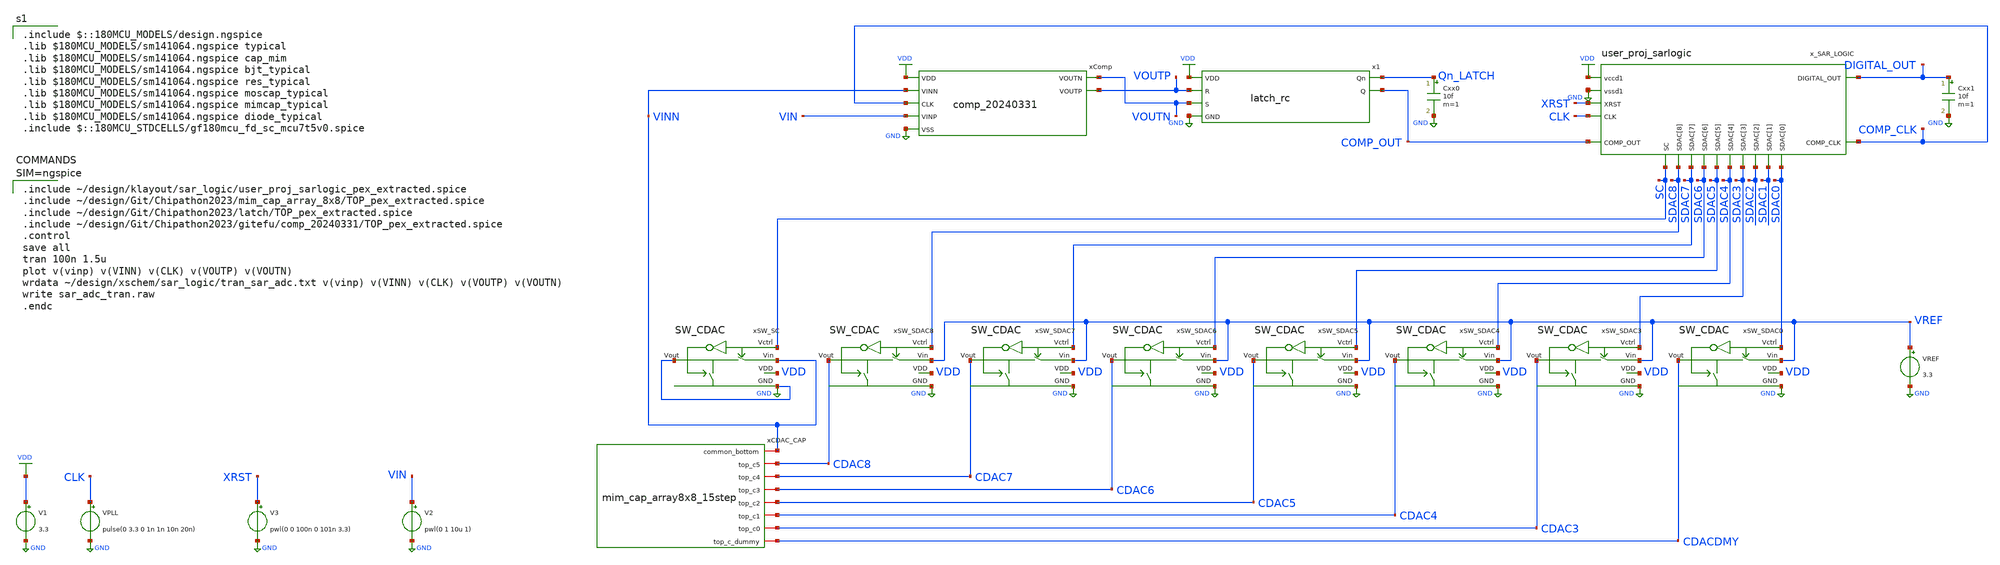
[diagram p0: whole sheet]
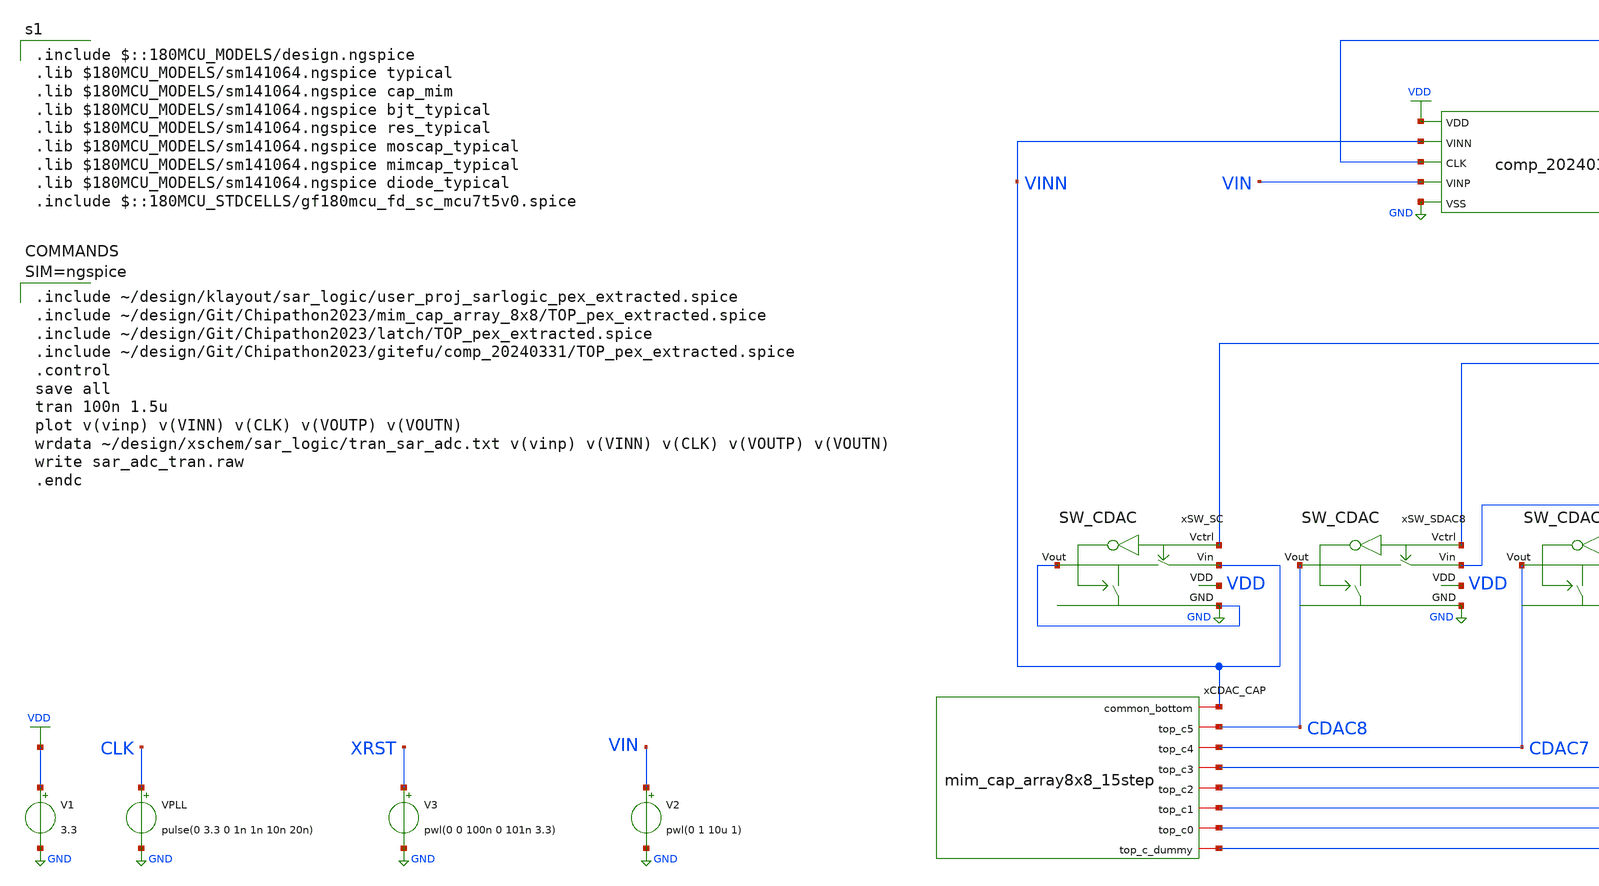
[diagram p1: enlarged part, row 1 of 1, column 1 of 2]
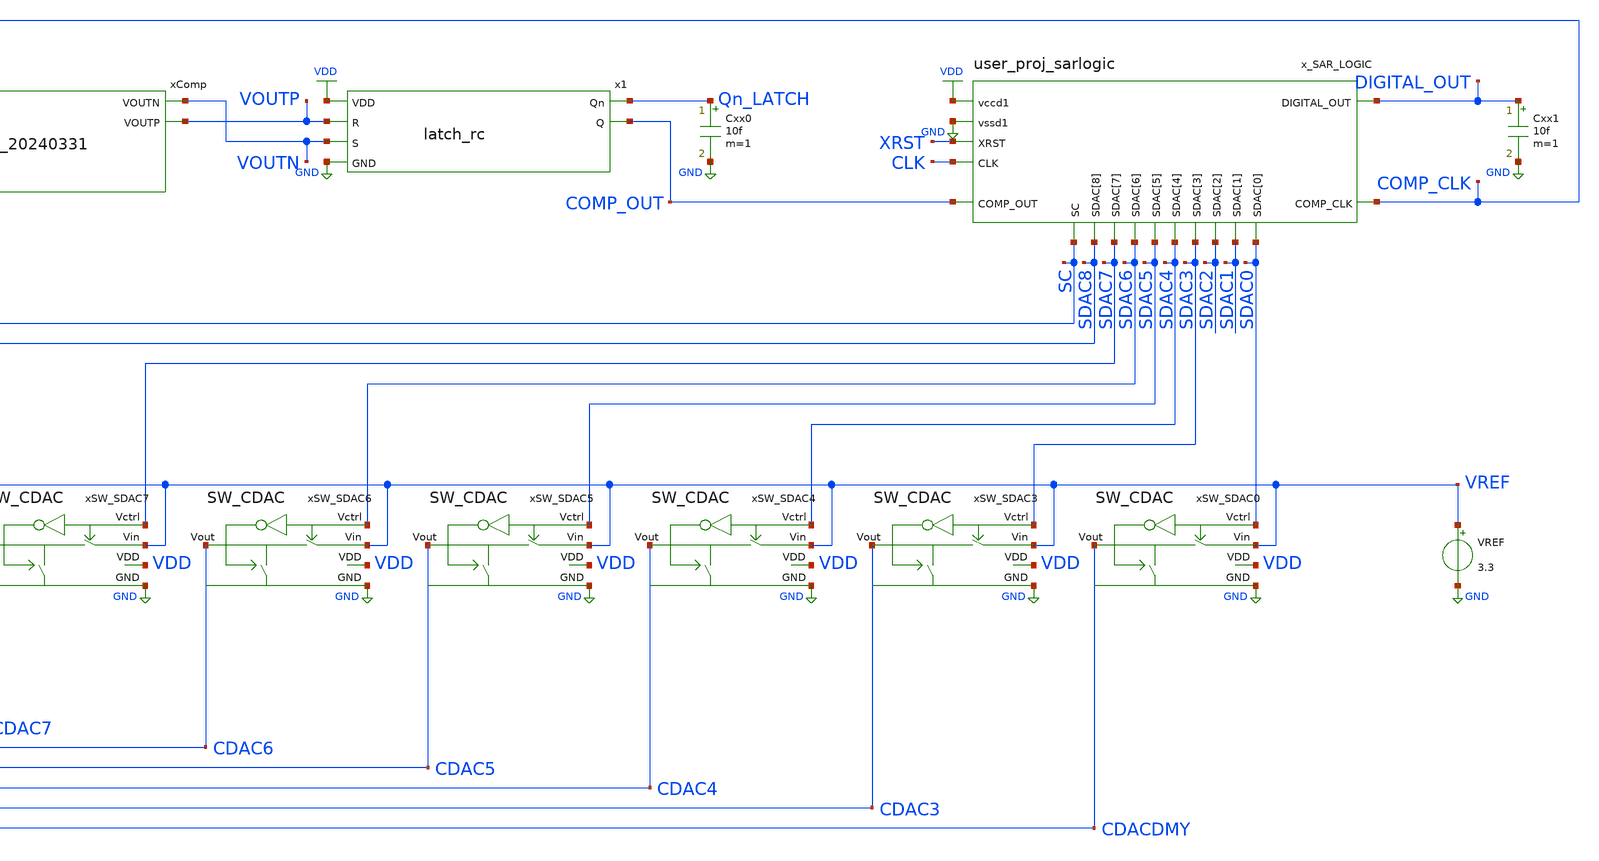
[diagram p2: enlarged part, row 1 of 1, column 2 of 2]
** sch_path: maple0705/SAR_ADC/tran_sar_adc.sch
**.subckt tran_sar_adc
V1 VDD GND 3.3
VPLL CLK GND pulse(0 3.3 0 1n 1n 10n 20n)
x_SAR_LOGIC CLK SC SDAC0 SDAC1 SDAC2 SDAC3 SDAC4 SDAC5 SDAC6 SDAC7 SDAC8 XRST COMP_CLK COMP_OUT
+ DIGITAL_OUT VDD GND user_proj_sarlogic
V3 XRST GND pwl(0 0 100n 0 101n 3.3)
xCDAC_CAP VINN CDAC5 CDAC6 CDAC7 CDAC8 CDACDMY CDAC4 CDAC3 CAP_ARRAY
xComp VDD COMP_CLK VOUTP VOUTN VIN VINN GND COMP
xSW_SDAC0 VDD SDAC0 GND CDACDMY VREF SW_CDAC
xSW_SDAC3 VDD SDAC3 GND CDAC3 VREF SW_CDAC
xSW_SDAC4 VDD SDAC4 GND CDAC4 VREF SW_CDAC
xSW_SDAC5 VDD SDAC5 GND CDAC5 VREF SW_CDAC
xSW_SDAC6 VDD SDAC6 GND CDAC6 VREF SW_CDAC
xSW_SDAC7 VDD SDAC7 GND CDAC7 VREF SW_CDAC
xSW_SDAC8 VDD SDAC8 GND CDAC8 VREF SW_CDAC
xSW_SC VDD SC GND GND VINN SW_CDAC
VREF VREF GND 3.3
Cxx0 Qn_LATCH GND 10f m=1
Cxx1 DIGITAL_OUT GND 10f m=1
V2 VIN GND pwl(0 1 10u 1)
x1 VOUTN VOUTP VDD GND Qn_LATCH COMP_OUT LATCH
**** begin user architecture code


.include ~/design/klayout/sar_logic/user_proj_sarlogic_pex_extracted.spice
.include ~/design/Git/Chipathon2023/mim_cap_array_8x8/TOP_pex_extracted.spice
.include ~/design/Git/Chipathon2023/latch/TOP_pex_extracted.spice
.include ~/design/Git/Chipathon2023/gitefu/comp_20240331/TOP_pex_extracted.spice
.control
save all
tran 100n 1.5u
plot v(vinp) v(VINN) v(CLK) v(VOUTP) v(VOUTN)
wrdata ~/design/xschem/sar_logic/tran_sar_adc.txt v(vinp) v(VINN) v(CLK) v(VOUTP) v(VOUTN)
write sar_adc_tran.raw
.endc



 .include $::180MCU_MODELS/design.ngspice
.lib $180MCU_MODELS/sm141064.ngspice typical
.lib $180MCU_MODELS/sm141064.ngspice cap_mim
.lib $180MCU_MODELS/sm141064.ngspice bjt_typical
.lib $180MCU_MODELS/sm141064.ngspice res_typical
.lib $180MCU_MODELS/sm141064.ngspice moscap_typical
.lib $180MCU_MODELS/sm141064.ngspice mimcap_typical
.lib $180MCU_MODELS/sm141064.ngspice diode_typical
.include $::180MCU_STDCELLS/gf180mcu_fd_sc_mcu7t5v0.spice
**** end user architecture code
**.ends
.GLOBAL GND
.GLOBAL VDD
.end
